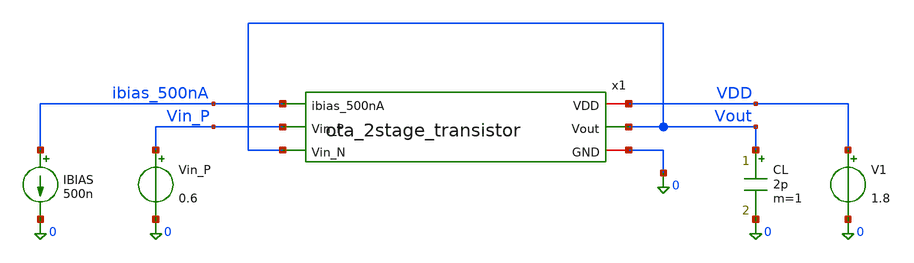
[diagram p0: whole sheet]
** sch_path: dfii/project_2stage_OTA_sim/tb_ota_2stage_dc.sch
**.subckt tb_ota_2stage_dc
x1 VDD ibias_500nA Vout Vin_P Vout 0 ota_2stage_transistor
V1 VDD 0 1.8
IBIAS ibias_500nA 0 500n
Vin_P Vin_P 0 0.6
CL Vout 0 2p m=1
**** begin user architecture code



.lib /foss/pdks/sky130A/libs.tech/ngspice/sky130.lib.spice tt

.control

op

* ============================================================
* Important DC nodes
* ============================================================

print v(Vout)
print v(x1.out_s1)
print v(x1.vdiode_n)
print v(x1.VCM)
print v(ibias_500nA)

let verr = v(Vin_P)-v(Vout)

print v(Vin_P)
print v(Vout)
print verr

* ============================================================
* PTAIL_0
* ============================================================

let id_pt0    = abs(@m.x1.xptail_0.msky130_fd_pr__pfet_01v8[id])
let gm_pt0    = abs(@m.x1.xptail_0.msky130_fd_pr__pfet_01v8[gm])
let gds_pt0   = abs(@m.x1.xptail_0.msky130_fd_pr__pfet_01v8[gds])
let gmid_pt0  = gm_pt0/id_pt0
let gain_pt0  = gm_pt0/gds_pt0
let vth_pt0   = abs(@m.x1.xptail_0.msky130_fd_pr__pfet_01v8[vth])
let vdsat_pt0 = abs(@m.x1.xptail_0.msky130_fd_pr__pfet_01v8[vdsat])

print id_pt0 gm_pt0 gds_pt0 gmid_pt0 gain_pt0 vth_pt0 vdsat_pt0


* ============================================================
* PTAIL_1
* ============================================================

let id_pt1    = abs(@m.x1.xptail_1.msky130_fd_pr__pfet_01v8[id])
let gm_pt1    = abs(@m.x1.xptail_1.msky130_fd_pr__pfet_01v8[gm])
let gds_pt1   = abs(@m.x1.xptail_1.msky130_fd_pr__pfet_01v8[gds])
let gmid_pt1  = gm_pt1/id_pt1
let gain_pt1  = gm_pt1/gds_pt1
let vdsat_pt1 = abs(@m.x1.xptail_1.msky130_fd_pr__pfet_01v8[vdsat])

print id_pt1 gm_pt1 gds_pt1 gmid_pt1 gain_pt1 vdsat_pt1


* ============================================================
* PDIFF_N
* ============================================================

let id_pdn    = abs(@m.x1.xpdiff_n.msky130_fd_pr__pfet_01v8[id])
let gm_pdn    = abs(@m.x1.xpdiff_n.msky130_fd_pr__pfet_01v8[gm])
let gds_pdn   = abs(@m.x1.xpdiff_n.msky130_fd_pr__pfet_01v8[gds])
let gmid_pdn  = gm_pdn/id_pdn
let gain_pdn  = gm_pdn/gds_pdn
let vdsat_pdn = abs(@m.x1.xpdiff_n.msky130_fd_pr__pfet_01v8[vdsat])

print id_pdn gm_pdn gds_pdn gmid_pdn gain_pdn vdsat_pdn


* ============================================================
* PDIFF_P
* ============================================================

let id_pdp    = abs(@m.x1.xpdiff_p.msky130_fd_pr__pfet_01v8[id])
let gm_pdp    = abs(@m.x1.xpdiff_p.msky130_fd_pr__pfet_01v8[gm])
let gds_pdp   = abs(@m.x1.xpdiff_p.msky130_fd_pr__pfet_01v8[gds])
let gmid_pdp  = gm_pdp/id_pdp
let gain_pdp  = gm_pdp/gds_pdp
let vdsat_pdp = abs(@m.x1.xpdiff_p.msky130_fd_pr__pfet_01v8[vdsat])

print id_pdp gm_pdp gds_pdp gmid_pdp gain_pdp vdsat_pdp


* ============================================================
* NLOAD_0
* ============================================================

let id_n0    = abs(@m.x1.xnload_0.msky130_fd_pr__nfet_01v8[id])
let gm_n0    = abs(@m.x1.xnload_0.msky130_fd_pr__nfet_01v8[gm])
let gds_n0   = abs(@m.x1.xnload_0.msky130_fd_pr__nfet_01v8[gds])
let gmid_n0  = gm_n0/id_n0
let gain_n0  = gm_n0/gds_n0
let vdsat_n0 = abs(@m.x1.xnload_0.msky130_fd_pr__nfet_01v8[vdsat])

print id_n0 gm_n0 gds_n0 gmid_n0 gain_n0 vdsat_n0


* ============================================================
* NLOAD_1
* ============================================================

let id_n1    = abs(@m.x1.xnload_1.msky130_fd_pr__nfet_01v8[id])
let gm_n1    = abs(@m.x1.xnload_1.msky130_fd_pr__nfet_01v8[gm])
let gds_n1   = abs(@m.x1.xnload_1.msky130_fd_pr__nfet_01v8[gds])
let gmid_n1  = gm_n1/id_n1
let gain_n1  = gm_n1/gds_n1
let vdsat_n1 = abs(@m.x1.xnload_1.msky130_fd_pr__nfet_01v8[vdsat])

print id_n1 gm_n1 gds_n1 gmid_n1 gain_n1 vdsat_n1


* ============================================================
* PTAIL_2
* ============================================================

let id_pt2    = abs(@m.x1.xptail_2.msky130_fd_pr__pfet_01v8[id])
let gm_pt2    = abs(@m.x1.xptail_2.msky130_fd_pr__pfet_01v8[gm])
let gds_pt2   = abs(@m.x1.xptail_2.msky130_fd_pr__pfet_01v8[gds])
let gmid_pt2  = gm_pt2/id_pt2
let gain_pt2  = gm_pt2/gds_pt2
let vdsat_pt2 = abs(@m.x1.xptail_2.msky130_fd_pr__pfet_01v8[vdsat])

print id_pt2 gm_pt2 gds_pt2 gmid_pt2 gain_pt2 vdsat_pt2


* ============================================================
* NLOAD_2
* ============================================================

let id_n2    = abs(@m.x1.xnload_2.msky130_fd_pr__nfet_01v8[id])
let gm_n2    = abs(@m.x1.xnload_2.msky130_fd_pr__nfet_01v8[gm])
let gds_n2   = abs(@m.x1.xnload_2.msky130_fd_pr__nfet_01v8[gds])
let gmid_n2  = gm_n2/id_n2
let gain_n2  = gm_n2/gds_n2
let vdsat_n2 = abs(@m.x1.xnload_2.msky130_fd_pr__nfet_01v8[vdsat])

print id_n2 gm_n2 gds_n2 gmid_n2 gain_n2 vdsat_n2

.endc



**** end user architecture code
**.ends

* expanding   symbol:
*+  /foss/designs/project_2stage_OTA/dfii/project_2stage_OTA/ota_2stage_transistor.sym # of pins=6
** sym_path: dfii/project_2stage_OTA/ota_2stage_transistor.sym
** sch_path: dfii/project_2stage_OTA/ota_2stage_transistor.sch
.subckt ota_2stage_transistor VDD ibias_500nA Vout Vin_P Vin_N GND
*.iopin VDD
*.iopin GND
*.ipin ibias_500nA
*.ipin Vin_N
*.ipin Vin_P
*.opin Vout
XNLOAD_0 vdiode_n vdiode_n GND GND sky130_fd_pr__nfet_01v8 L=12 W=3.6 nf=1 ad='int((1 + 1)/2) * 3.6 / 1 * 0.29'
+ as='int((1 + 2)/2) * 3.6 / 1 * 0.29' pd='2*int((1 + 1)/2) * (3.6 / 1 + 0.29)' ps='2*int((1 + 2)/2) * (3.6 / 1 + 0.29)'
+ nrd='0.29 / 3.6 ' nrs='0.29 / 3.6 ' sa=0 sb=0 sd=0 mult=1 m=1
XNLOAD_1 out_s1 vdiode_n GND GND sky130_fd_pr__nfet_01v8 L=12 W=3.6 nf=1 ad='int((1 + 1)/2) * 3.6 / 1 * 0.29'
+ as='int((1 + 2)/2) * 3.6 / 1 * 0.29' pd='2*int((1 + 1)/2) * (3.6 / 1 + 0.29)' ps='2*int((1 + 2)/2) * (3.6 / 1 + 0.29)'
+ nrd='0.29 / 3.6 ' nrs='0.29 / 3.6 ' sa=0 sb=0 sd=0 mult=1 m=1
XNLOAD_2 Vout out_s1 GND GND sky130_fd_pr__nfet_01v8 L=2 W=3.6 nf=1 ad='int((1 + 1)/2) * 3.6 / 1 * 0.29'
+ as='int((1 + 2)/2) * 3.6 / 1 * 0.29' pd='2*int((1 + 1)/2) * (3.6 / 1 + 0.29)' ps='2*int((1 + 2)/2) * (3.6 / 1 + 0.29)'
+ nrd='0.29 / 3.6 ' nrs='0.29 / 3.6 ' sa=0 sb=0 sd=0 mult=2 m=2
XPDIFF_N vdiode_n Vin_N VCM VCM sky130_fd_pr__pfet_01v8 L=1 W=7.4 nf=1 ad='int((1 + 1)/2) * 7.4 / 1 * 0.29'
+ as='int((1 + 2)/2) * 7.4 / 1 * 0.29' pd='2*int((1 + 1)/2) * (7.4 / 1 + 0.29)' ps='2*int((1 + 2)/2) * (7.4 / 1 + 0.29)'
+ nrd='0.29 / 7.4 ' nrs='0.29 / 7.4 ' sa=0 sb=0 sd=0 mult=12 m=12
XPDIFF_P out_s1 Vin_P VCM VCM sky130_fd_pr__pfet_01v8 L=1 W=7.4 nf=1 ad='int((1 + 1)/2) * 7.4 / 1 * 0.29'
+ as='int((1 + 2)/2) * 7.4 / 1 * 0.29' pd='2*int((1 + 1)/2) * (7.4 / 1 + 0.29)' ps='2*int((1 + 2)/2) * (7.4 / 1 + 0.29)'
+ nrd='0.29 / 7.4 ' nrs='0.29 / 7.4 ' sa=0 sb=0 sd=0 mult=12 m=12
XPTAIL_1 VCM ibias_500nA VDD VDD sky130_fd_pr__pfet_01v8 L=1 W=1.76 nf=1 ad='int((1 + 1)/2) * 1.76 / 1 * 0.29'
+ as='int((1 + 2)/2) * 1.76 / 1 * 0.29' pd='2*int((1 + 1)/2) * (1.76 / 1 + 0.29)' ps='2*int((1 + 2)/2) * (1.76 / 1 + 0.29)'
+ nrd='0.29 / 1.76 ' nrs='0.29 / 1.76 ' sa=0 sb=0 sd=0 mult=1 m=1
XPTAIL_2 Vout ibias_500nA VDD VDD sky130_fd_pr__pfet_01v8 L=1 W=1.76 nf=1 ad='int((1 + 1)/2) * 1.76 / 1 * 0.29'
+ as='int((1 + 2)/2) * 1.76 / 1 * 0.29' pd='2*int((1 + 1)/2) * (1.76 / 1 + 0.29)' ps='2*int((1 + 2)/2) * (1.76 / 1 + 0.29)'
+ nrd='0.29 / 1.76 ' nrs='0.29 / 1.76 ' sa=0 sb=0 sd=0 mult=6 m=6
XPTAIL_0 ibias_500nA ibias_500nA VDD VDD sky130_fd_pr__pfet_01v8 L=1 W=1.76 nf=1 ad='int((1 + 1)/2) * 1.76 / 1 * 0.29'
+ as='int((1 + 2)/2) * 1.76 / 1 * 0.29' pd='2*int((1 + 1)/2) * (1.76 / 1 + 0.29)' ps='2*int((1 + 2)/2) * (1.76 / 1 + 0.29)'
+ nrd='0.29 / 1.76 ' nrs='0.29 / 1.76 ' sa=0 sb=0 sd=0 mult=1 m=1
XCMILLER out_s1 net1 sky130_fd_pr__cap_mim_m3_1 W=19 L=19 MF=1 m=1
XRMILLER Vout net1 GND sky130_fd_pr__res_xhigh_po_0p35 L=31.5 mult=1 m=1
.ends

.GLOBAL VDD
.end
